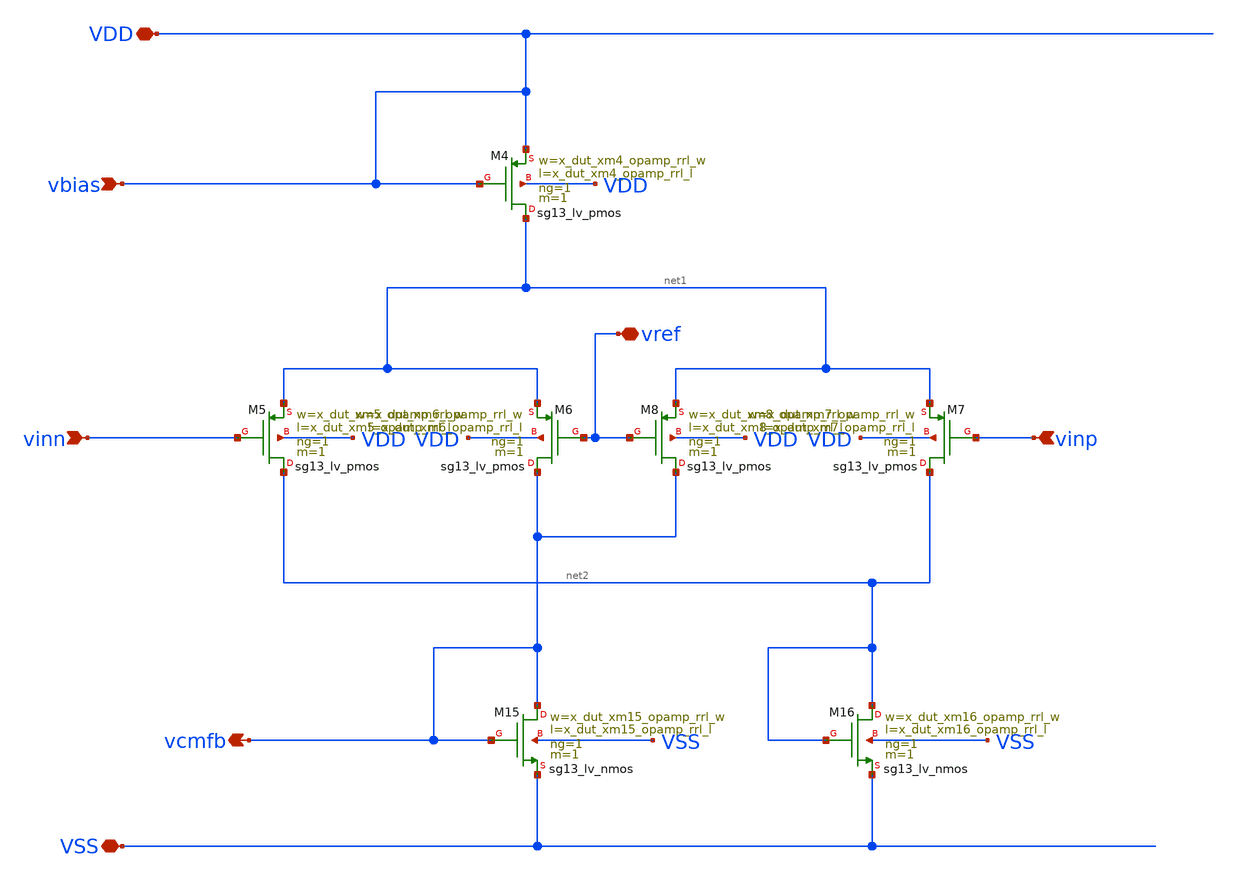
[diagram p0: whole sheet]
** sch_path: analog-db/drawings/shared/cmfb-output-diff-pair-sense.sch
* Copyright 2026 MacAnalog Research Group
**.subckt cmfb-output-diff-pair-sense VDD vinp vinn vbias vcmfb VSS vref
*.iopin VDD
*.ipin vinp
*.ipin vinn
*.ipin vbias
*.opin vcmfb
*.iopin VSS
*.iopin vref
XM4 net1 VDD VDD VDD sg13_lv_pmos w=x_dut_xm4_opamp_rrl_w l=x_dut_xm4_opamp_rrl_l ng=1 m=1 mm_ok=1
XM5 net2 vinn net1 VDD sg13_lv_pmos w=x_dut_xm5_opamp_rrl_w l=x_dut_xm5_opamp_rrl_l ng=1 m=1 mm_ok=1
XM6 vcmfb vref net1 VDD sg13_lv_pmos w=x_dut_xm6_opamp_rrl_w l=x_dut_xm6_opamp_rrl_l ng=1 m=1
+ mm_ok=1
XM7 net2 vinp net1 VDD sg13_lv_pmos w=x_dut_xm7_opamp_rrl_w l=x_dut_xm7_opamp_rrl_l ng=1 m=1 mm_ok=1
XM8 vcmfb vref net1 VDD sg13_lv_pmos w=x_dut_xm8_opamp_rrl_w l=x_dut_xm8_opamp_rrl_l ng=1 m=1
+ mm_ok=1
XM15 vcmfb vcmfb VSS VSS sg13_lv_nmos w=x_dut_xm15_opamp_rrl_w l=x_dut_xm15_opamp_rrl_l ng=1 m=1
+ mm_ok=1
XM16 net2 net2 VSS VSS sg13_lv_nmos w=x_dut_xm16_opamp_rrl_w l=x_dut_xm16_opamp_rrl_l ng=1 m=1
+ mm_ok=1
**.ends
.end
